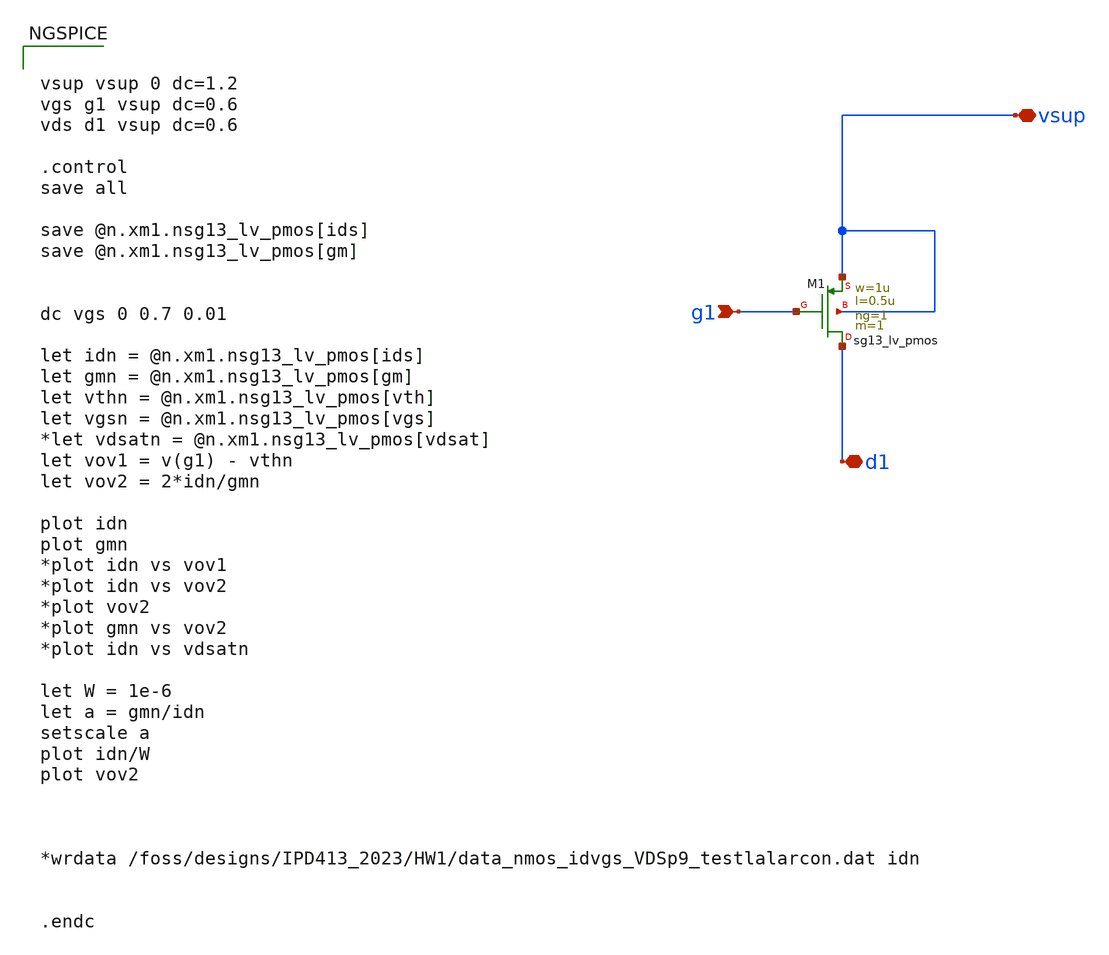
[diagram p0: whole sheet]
** sch_path: xschem/Tareas/Tarea_2/pmos_charac_IPD413HW2_LVT_IHP.sch
**.subckt pmos_charac_IPD413HW2_LVT_IHP g1 d1 vsup
*.ipin g1
*.iopin d1
*.iopin vsup
XM1 d1 g1 vsup vsup sg13_lv_pmos w=1u l=0.5u ng=1 m=1 mm_ok=1
**** begin user architecture code


vsup vsup 0 dc=1.2
vgs g1 vsup dc=0.6
vds d1 vsup dc=0.6

.control
save all

save @n.xm1.nsg13_lv_pmos[ids]
save @n.xm1.nsg13_lv_pmos[gm]


dc vgs 0 0.7 0.01

let idn = @n.xm1.nsg13_lv_pmos[ids]
let gmn = @n.xm1.nsg13_lv_pmos[gm]
let vthn = @n.xm1.nsg13_lv_pmos[vth]
let vgsn = @n.xm1.nsg13_lv_pmos[vgs]
*let vdsatn = @n.xm1.nsg13_lv_pmos[vdsat]
let vov1 = v(g1) - vthn
let vov2 = 2*idn/gmn

plot idn
plot gmn
*plot idn vs vov1
*plot idn vs vov2
*plot vov2
*plot gmn vs vov2
*plot idn vs vdsatn

let W = 1e-6
let a = gmn/idn
setscale a
plot idn/W
plot vov2



*wrdata /foss/designs/IPD413_2023/HW1/data_nmos_idvgs_VDSp9_testlalarcon.dat idn


.endc




.lib cornerMOShv.lib mos_tt
.lib cornerMOSlv.lib mos_tt
*.lib cornerMOShv.lib mos_ff
*.lib cornerMOSlv.lib mos_ff
*.lib cornerMOShv.lib mos_ss
*.lib cornerMOSlv.lib mos_ss
*.lib cornerMOShv.lib mos_sf
*.lib cornerMOSlv.lib mos_sf
*.lib cornerMOShv.lib mos_fs
*.lib cornerMOSlv.lib mos_fs

.include /opt/pdks/ihp-sg13g2/libs.ref/sg13g2_stdcell/spice/sg13g2_stdcell.spice
.lib $::SG13G2_MODELS/cornerRES.lib res_typ
.lib $::SG13G2_MODELS/cornerCAP.lib cap_typ
*.lib $::SG13G2_MODELS/diodes.lib

**** end user architecture code
**.ends
.end
